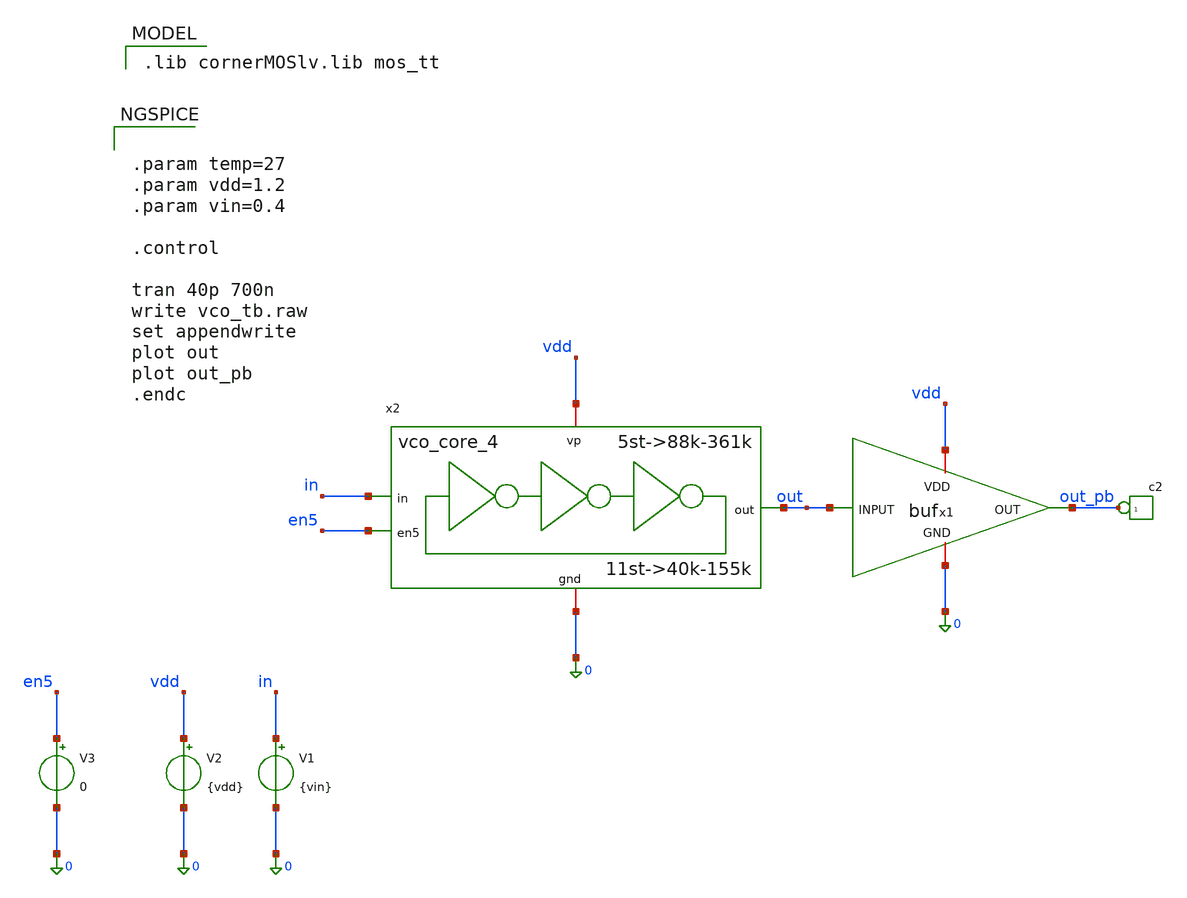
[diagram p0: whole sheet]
** sch_path: schematics/vco/vco_tb/vco_dcin_tb.sch
**.subckt vco_dcin_tb
V1 in 0 {vin}
V2 vdd 0 {vdd}
*connector(1,1) ?1 out_pb
x1 vdd out out_pb 0 buf
x2 vdd 0 out en5 in vco_core_4
V3 en5 0 0
**** begin user architecture code


.param temp=27
.param vdd=1.2
.param vin=0.4

.control

tran 40p 700n
write vco_tb.raw
set appendwrite
plot out
plot out_pb
.endc


 .lib cornerMOSlv.lib mos_tt

**** end user architecture code
**.ends
.end
